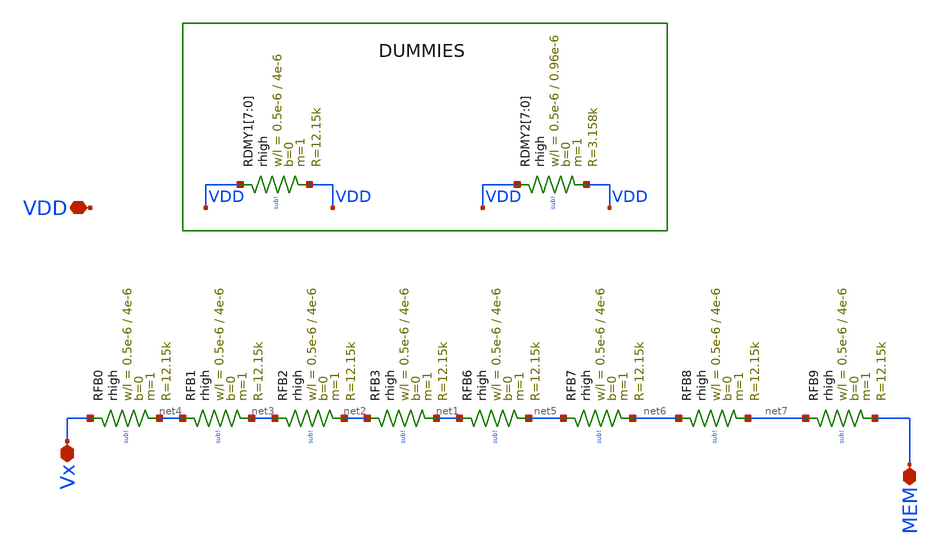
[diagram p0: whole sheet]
** sch_path: OSC9996-main/schematic/xschem/resistence_bank.sch
**.subckt resistence_bank VDD Vx MEM
*.iopin VDD
*.iopin Vx
*.iopin MEM
XRFB0 Vx net4 sub! rhigh w=0.5e-6 l=4e-6 m=1 b=0 mm_ok=1
XRFB1 net4 net3 sub! rhigh w=0.5e-6 l=4e-6 m=1 b=0 mm_ok=1
XRFB2 net3 net2 sub! rhigh w=0.5e-6 l=4e-6 m=1 b=0 mm_ok=1
XRFB3 net2 net1 sub! rhigh w=0.5e-6 l=4e-6 m=1 b=0 mm_ok=1
XRDMY1[7] VDD VDD sub! rhigh w=0.5e-6 l=4e-6 m=1 b=0 mm_ok=1
XRDMY1[6] VDD VDD sub! rhigh w=0.5e-6 l=4e-6 m=1 b=0 mm_ok=1
XRDMY1[5] VDD VDD sub! rhigh w=0.5e-6 l=4e-6 m=1 b=0 mm_ok=1
XRDMY1[4] VDD VDD sub! rhigh w=0.5e-6 l=4e-6 m=1 b=0 mm_ok=1
XRDMY1[3] VDD VDD sub! rhigh w=0.5e-6 l=4e-6 m=1 b=0 mm_ok=1
XRDMY1[2] VDD VDD sub! rhigh w=0.5e-6 l=4e-6 m=1 b=0 mm_ok=1
XRDMY1[1] VDD VDD sub! rhigh w=0.5e-6 l=4e-6 m=1 b=0 mm_ok=1
XRDMY1[0] VDD VDD sub! rhigh w=0.5e-6 l=4e-6 m=1 b=0 mm_ok=1
XRFB6 net1 net5 sub! rhigh w=0.5e-6 l=4e-6 m=1 b=0 mm_ok=1
XRFB7 net5 net6 sub! rhigh w=0.5e-6 l=4e-6 m=1 b=0 mm_ok=1
XRFB8 net6 net7 sub! rhigh w=0.5e-6 l=4e-6 m=1 b=0 mm_ok=1
XRFB9 net7 MEM sub! rhigh w=0.5e-6 l=4e-6 m=1 b=0 mm_ok=1
XRDMY2[7] VDD VDD sub! rhigh w=0.5e-6 l=0.96e-6 m=1 b=0 mm_ok=1
XRDMY2[6] VDD VDD sub! rhigh w=0.5e-6 l=0.96e-6 m=1 b=0 mm_ok=1
XRDMY2[5] VDD VDD sub! rhigh w=0.5e-6 l=0.96e-6 m=1 b=0 mm_ok=1
XRDMY2[4] VDD VDD sub! rhigh w=0.5e-6 l=0.96e-6 m=1 b=0 mm_ok=1
XRDMY2[3] VDD VDD sub! rhigh w=0.5e-6 l=0.96e-6 m=1 b=0 mm_ok=1
XRDMY2[2] VDD VDD sub! rhigh w=0.5e-6 l=0.96e-6 m=1 b=0 mm_ok=1
XRDMY2[1] VDD VDD sub! rhigh w=0.5e-6 l=0.96e-6 m=1 b=0 mm_ok=1
XRDMY2[0] VDD VDD sub! rhigh w=0.5e-6 l=0.96e-6 m=1 b=0 mm_ok=1
**.ends
.end
